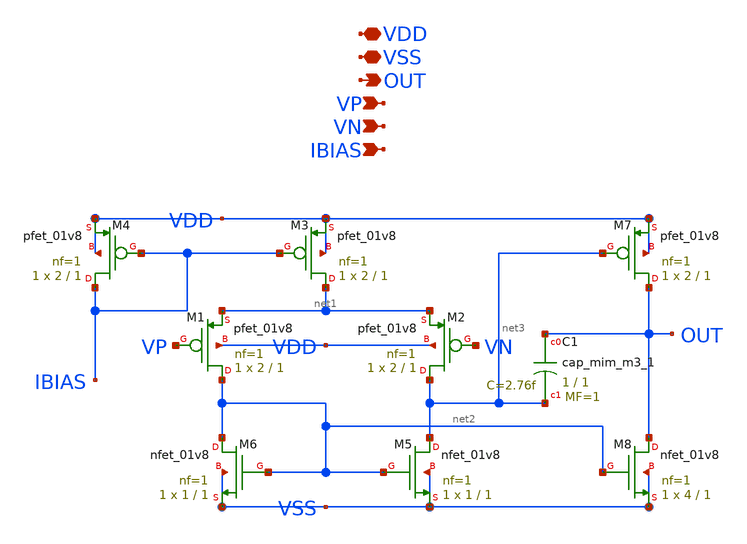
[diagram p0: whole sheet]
** sch_path: designs/libs/core_analog/p-ota/2-stage-p-ota.sch
**.subckt 2-stage-p-ota VDD VSS VP VN OUT IBIAS
*.iopin VDD
*.iopin VSS
*.ipin VP
*.ipin VN
*.opin OUT
*.ipin IBIAS
XM1 net2 VP net1 VDD sky130_fd_pr__pfet_01v8 L=1 W=2 nf=1 ad='int((nf+1)/2) * W/nf * 0.29' as='int((nf+2)/2) * W/nf * 0.29'
+ pd='2*int((nf+1)/2) * (W/nf + 0.29)' ps='2*int((nf+2)/2) * (W/nf + 0.29)' nrd='0.29 / W' nrs='0.29 / W'
+ sa=0 sb=0 sd=0 mult=1 m=1
XM2 net3 VN net1 VDD sky130_fd_pr__pfet_01v8 L=1 W=2 nf=1 ad='int((nf+1)/2) * W/nf * 0.29' as='int((nf+2)/2) * W/nf * 0.29'
+ pd='2*int((nf+1)/2) * (W/nf + 0.29)' ps='2*int((nf+2)/2) * (W/nf + 0.29)' nrd='0.29 / W' nrs='0.29 / W'
+ sa=0 sb=0 sd=0 mult=1 m=1
XM3 net1 IBIAS VDD VDD sky130_fd_pr__pfet_01v8 L=1 W=2 nf=1 ad='int((nf+1)/2) * W/nf * 0.29' as='int((nf+2)/2) * W/nf * 0.29'
+ pd='2*int((nf+1)/2) * (W/nf + 0.29)' ps='2*int((nf+2)/2) * (W/nf + 0.29)' nrd='0.29 / W' nrs='0.29 / W'
+ sa=0 sb=0 sd=0 mult=1 m=1
XM4 IBIAS IBIAS VDD VDD sky130_fd_pr__pfet_01v8 L=1 W=2 nf=1 ad='int((nf+1)/2) * W/nf * 0.29' as='int((nf+2)/2) * W/nf * 0.29'
+ pd='2*int((nf+1)/2) * (W/nf + 0.29)' ps='2*int((nf+2)/2) * (W/nf + 0.29)' nrd='0.29 / W' nrs='0.29 / W'
+ sa=0 sb=0 sd=0 mult=1 m=1
XM5 net3 net2 VSS VSS sky130_fd_pr__nfet_01v8 L=1 W=1 nf=1 ad='int((nf+1)/2) * W/nf * 0.29' as='int((nf+2)/2) * W/nf * 0.29'
+ pd='2*int((nf+1)/2) * (W/nf + 0.29)' ps='2*int((nf+2)/2) * (W/nf + 0.29)' nrd='0.29 / W' nrs='0.29 / W'
+ sa=0 sb=0 sd=0 mult=1 m=1
XM6 net2 net2 VSS VSS sky130_fd_pr__nfet_01v8 L=1 W=1 nf=1 ad='int((nf+1)/2) * W/nf * 0.29' as='int((nf+2)/2) * W/nf * 0.29'
+ pd='2*int((nf+1)/2) * (W/nf + 0.29)' ps='2*int((nf+2)/2) * (W/nf + 0.29)' nrd='0.29 / W' nrs='0.29 / W'
+ sa=0 sb=0 sd=0 mult=1 m=1
XM7 OUT net3 VDD VDD sky130_fd_pr__pfet_01v8 L=1 W=2 nf=1 ad='int((nf+1)/2) * W/nf * 0.29' as='int((nf+2)/2) * W/nf * 0.29'
+ pd='2*int((nf+1)/2) * (W/nf + 0.29)' ps='2*int((nf+2)/2) * (W/nf + 0.29)' nrd='0.29 / W' nrs='0.29 / W'
+ sa=0 sb=0 sd=0 mult=1 m=1
XM8 OUT net2 VSS VSS sky130_fd_pr__nfet_01v8 L=1 W=4 nf=1 ad='int((nf+1)/2) * W/nf * 0.29' as='int((nf+2)/2) * W/nf * 0.29'
+ pd='2*int((nf+1)/2) * (W/nf + 0.29)' ps='2*int((nf+2)/2) * (W/nf + 0.29)' nrd='0.29 / W' nrs='0.29 / W'
+ sa=0 sb=0 sd=0 mult=1 m=1
XC1 OUT net3 sky130_fd_pr__cap_mim_m3_1 W=1 L=1 MF=1 m=1
**.ends
.end
